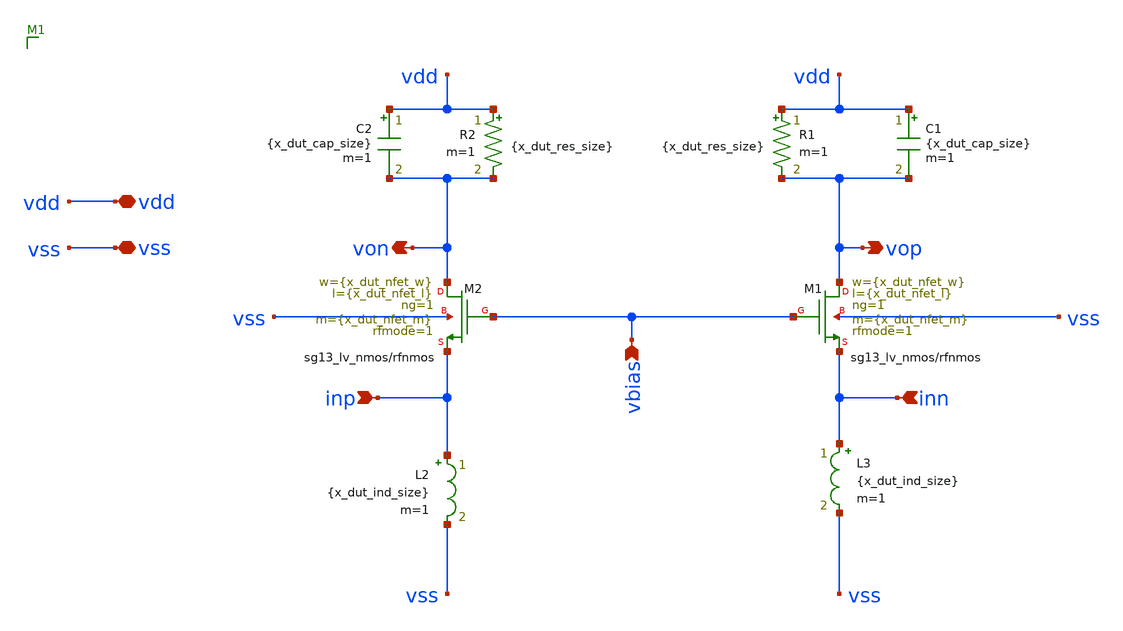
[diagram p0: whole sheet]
** sch_path: examples/tunable-tia/ihp-sg13g2/xschem/tia-topo-3/tia-bpf-3-ideal-component.sch
**.subckt tia-bpf-3-ideal-component vdd vss inp inn von vop vbias
*.iopin vdd
*.iopin vss
*.ipin inp
*.ipin inn
*.opin von
*.opin vop
*.ipin vbias
XM1 vop vbias inn vss sg13_lv_nmos w={x_dut_nfet_w} l={x_dut_nfet_l} ng=1 m={x_dut_nfet_m} rfmode=1 mm_ok=1
XM2 von vbias inp vss sg13_lv_nmos w={x_dut_nfet_w} l={x_dut_nfet_l} ng=1 m={x_dut_nfet_m} rfmode=1 mm_ok=1
L2 inp vss {x_dut_ind_size} m=1
L3 inn vss {x_dut_ind_size} m=1
R1 vdd vop {x_dut_res_size} m=1
R2 vdd von {x_dut_res_size} m=1
C1 vdd vop {x_dut_cap_size} m=1
C2 vdd von {x_dut_cap_size} m=1
**.ends
.end
